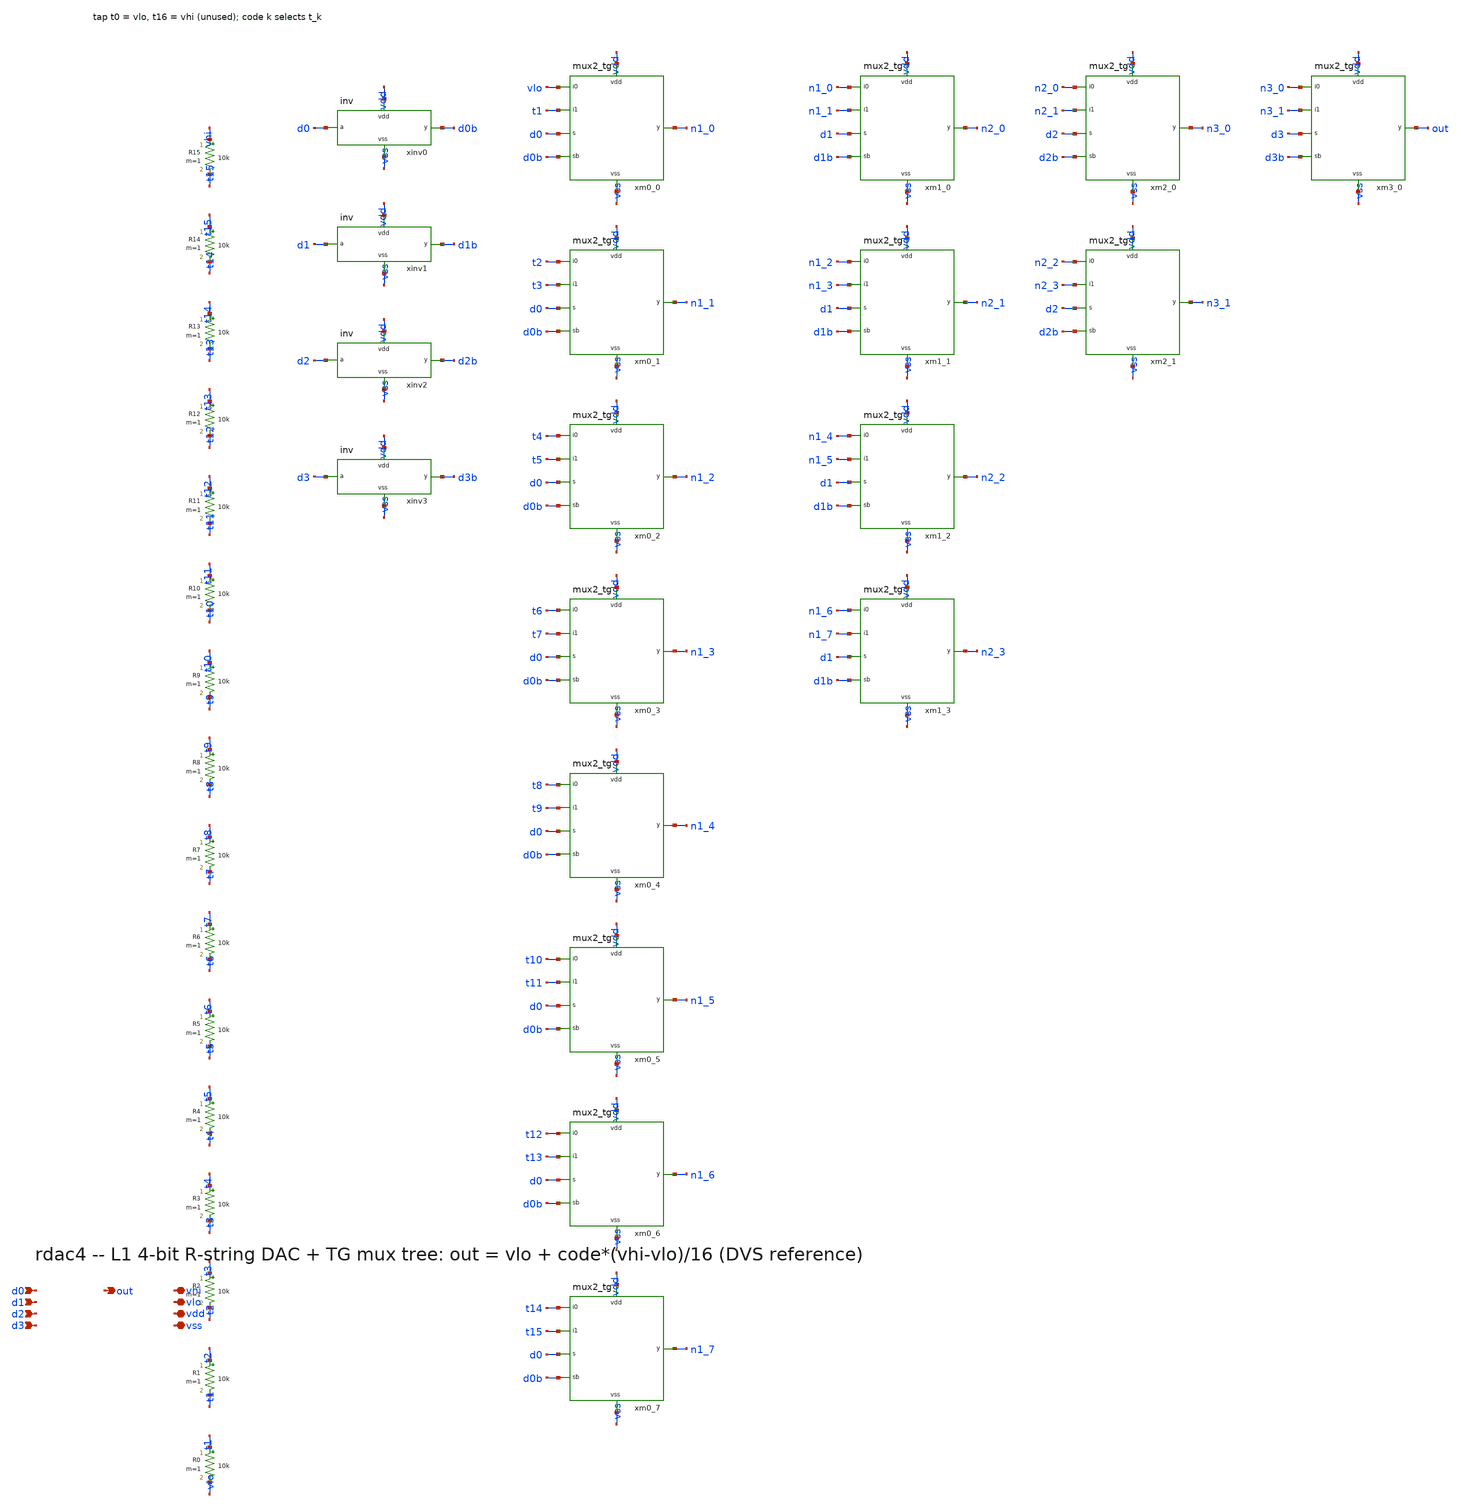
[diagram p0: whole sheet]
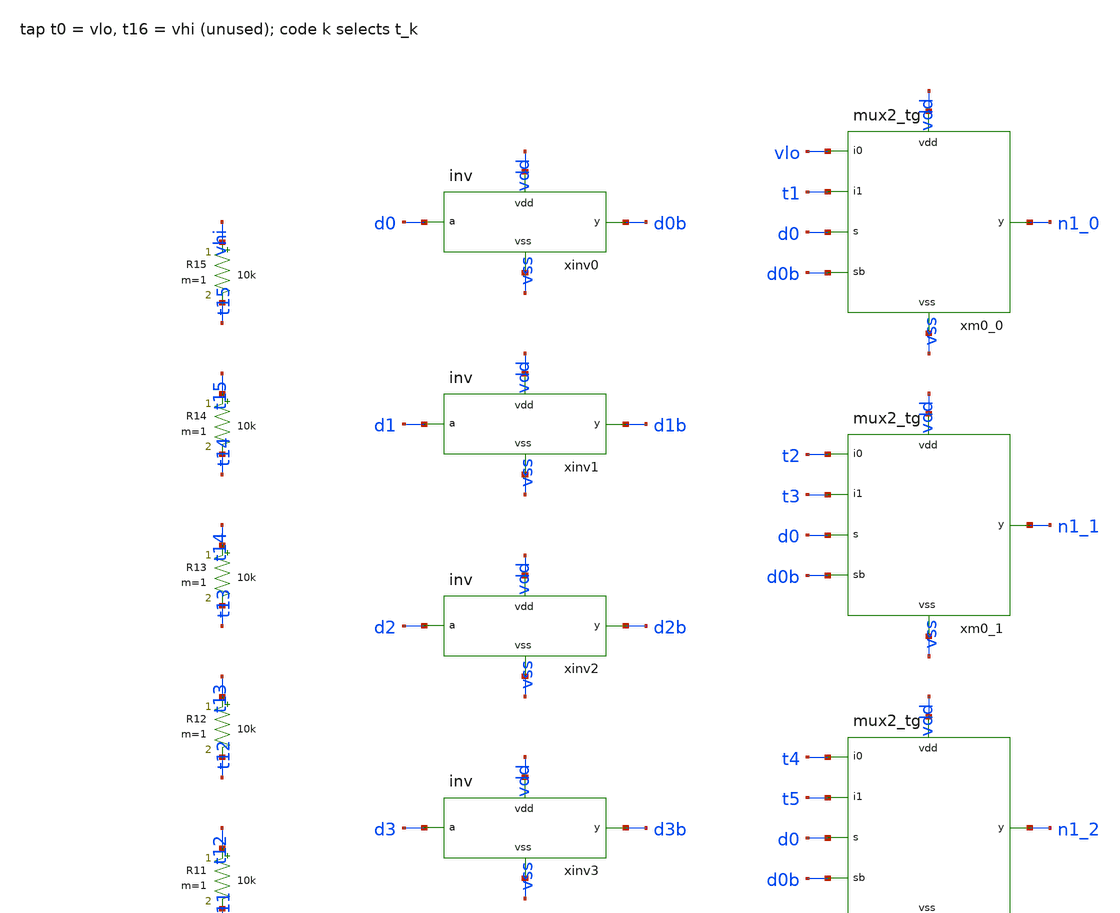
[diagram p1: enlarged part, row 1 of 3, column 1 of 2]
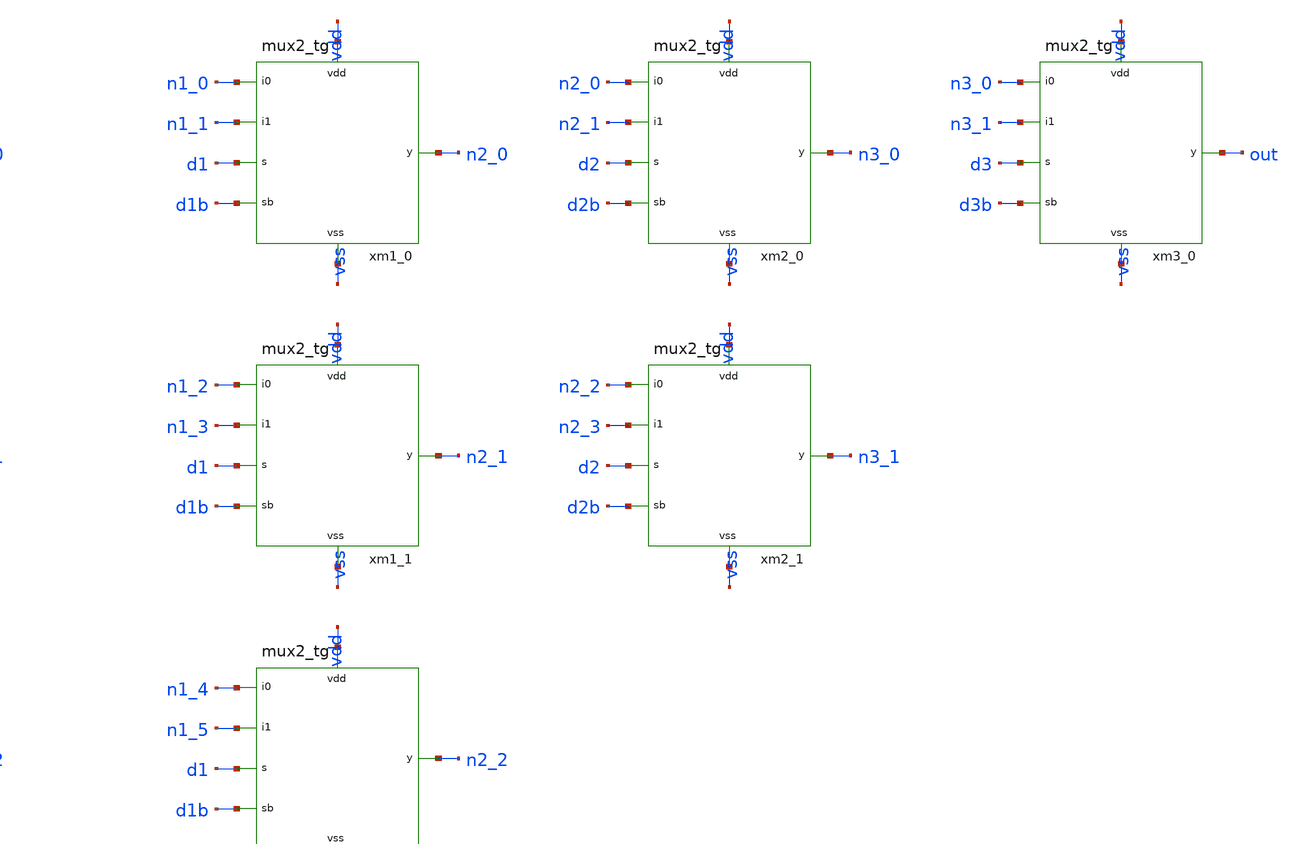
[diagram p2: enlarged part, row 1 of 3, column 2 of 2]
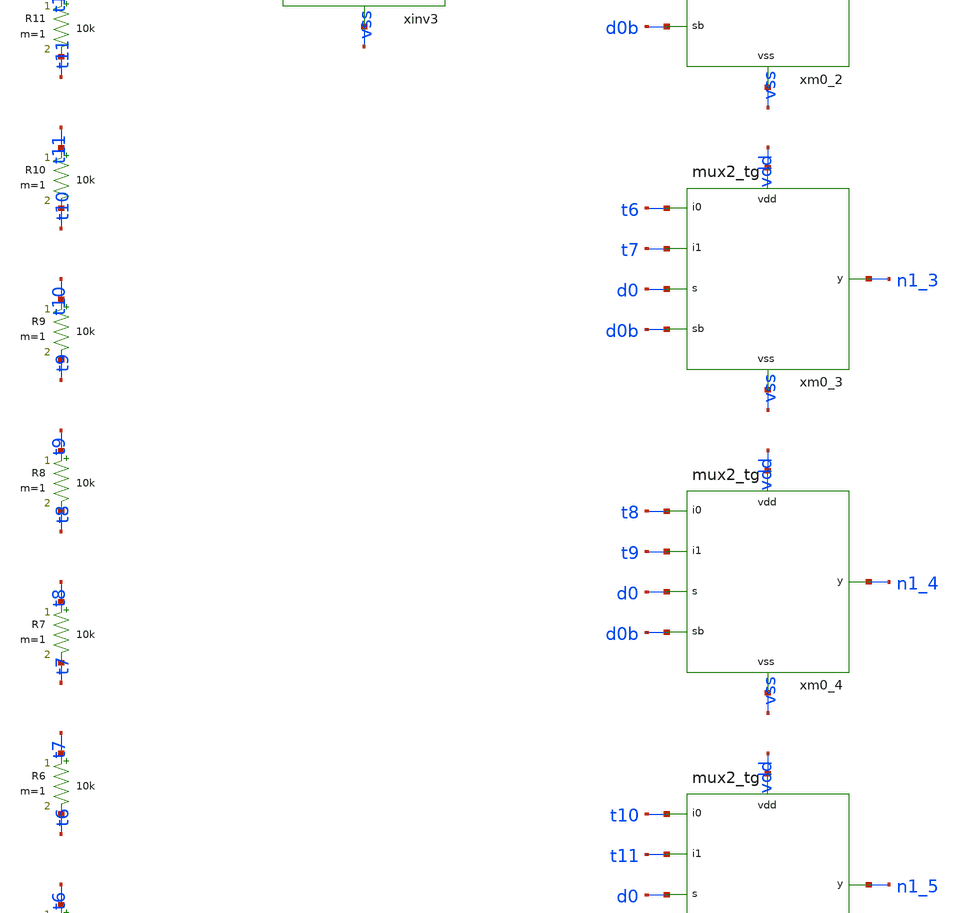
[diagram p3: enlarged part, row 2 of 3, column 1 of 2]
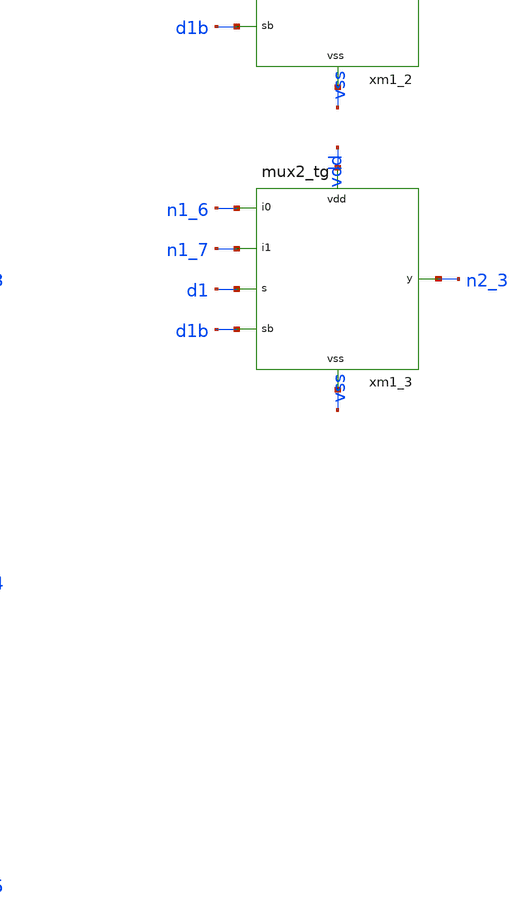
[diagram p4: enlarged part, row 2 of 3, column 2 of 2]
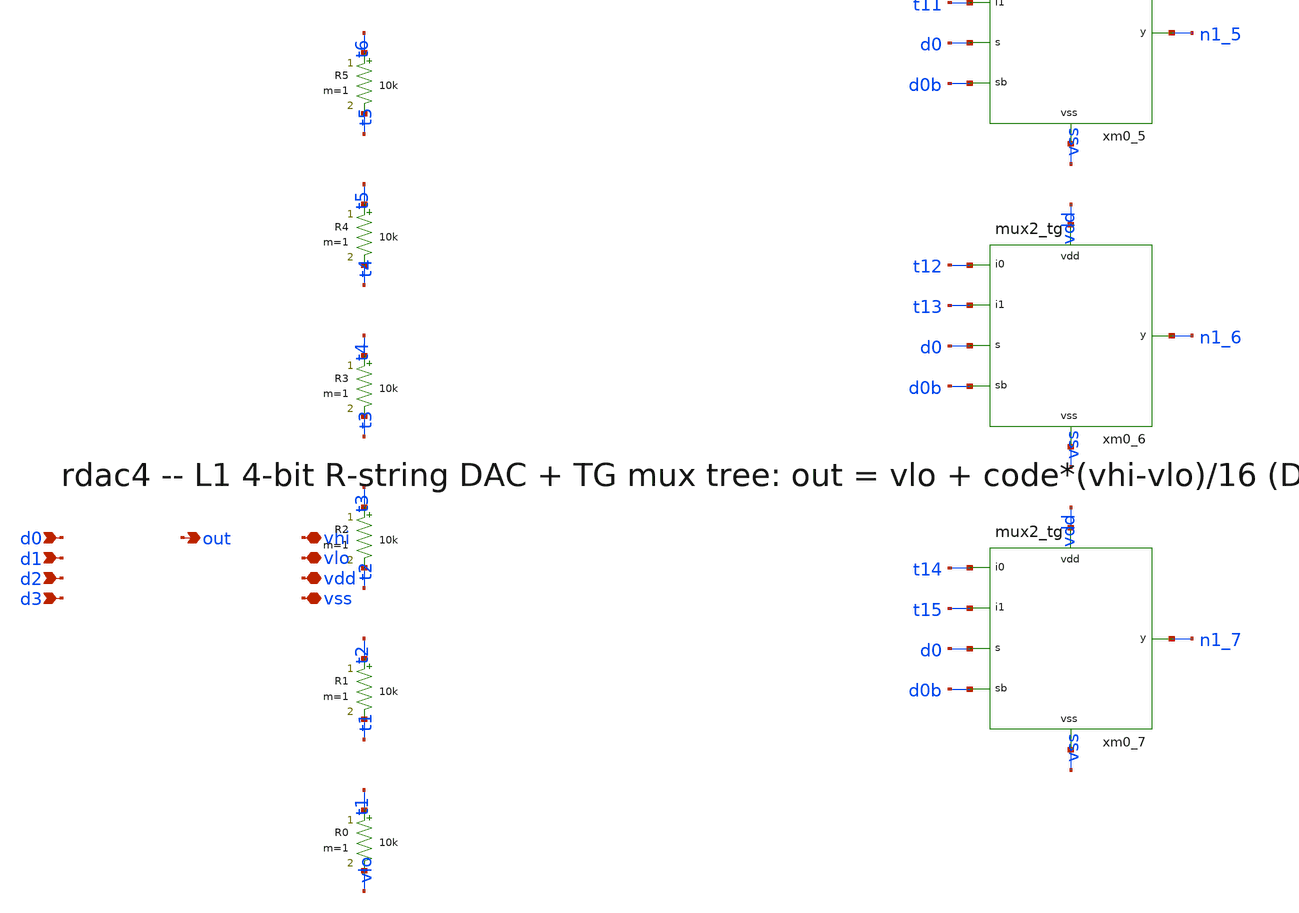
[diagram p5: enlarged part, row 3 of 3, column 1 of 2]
** sch_path: xschem/onetops/rdac4.sch
**.subckt rdac4 d0 d1 d2 d3 out vhi vlo vdd vss
*.ipin d0
*.ipin d1
*.ipin d2
*.ipin d3
*.opin out
*.iopin vhi
*.iopin vlo
*.iopin vdd
*.iopin vss
R0 t1 vlo 10k m=1
R1 t2 t1 10k m=1
R2 t3 t2 10k m=1
R3 t4 t3 10k m=1
R4 t5 t4 10k m=1
R5 t6 t5 10k m=1
R6 t7 t6 10k m=1
R7 t8 t7 10k m=1
R8 t9 t8 10k m=1
R9 t10 t9 10k m=1
R10 t11 t10 10k m=1
R11 t12 t11 10k m=1
R12 t13 t12 10k m=1
R13 t14 t13 10k m=1
R14 t15 t14 10k m=1
R15 vhi t15 10k m=1
xinv0 d0 d0b vdd vss inv
xinv1 d1 d1b vdd vss inv
xinv2 d2 d2b vdd vss inv
xinv3 d3 d3b vdd vss inv
xm0_0 vlo t1 d0 d0b n1_0 vdd vss mux2_tg
xm0_1 t2 t3 d0 d0b n1_1 vdd vss mux2_tg
xm0_2 t4 t5 d0 d0b n1_2 vdd vss mux2_tg
xm0_3 t6 t7 d0 d0b n1_3 vdd vss mux2_tg
xm0_4 t8 t9 d0 d0b n1_4 vdd vss mux2_tg
xm0_5 t10 t11 d0 d0b n1_5 vdd vss mux2_tg
xm0_6 t12 t13 d0 d0b n1_6 vdd vss mux2_tg
xm0_7 t14 t15 d0 d0b n1_7 vdd vss mux2_tg
xm1_0 n1_0 n1_1 d1 d1b n2_0 vdd vss mux2_tg
xm1_1 n1_2 n1_3 d1 d1b n2_1 vdd vss mux2_tg
xm1_2 n1_4 n1_5 d1 d1b n2_2 vdd vss mux2_tg
xm1_3 n1_6 n1_7 d1 d1b n2_3 vdd vss mux2_tg
xm2_0 n2_0 n2_1 d2 d2b n3_0 vdd vss mux2_tg
xm2_1 n2_2 n2_3 d2 d2b n3_1 vdd vss mux2_tg
xm3_0 n3_0 n3_1 d3 d3b out vdd vss mux2_tg
**.ends

* expanding   symbol:  onetops/inv.sym # of pins=4
** sym_path: xschem/onetops/inv.sym
** sch_path: xschem/onetops/inv.sch
.subckt inv a y vdd vss
*.ipin a
*.opin y
*.iopin vdd
*.iopin vss
XMP1 y a vdd vdd sky130_fd_pr__pfet_01v8 L=0.15 W=2 nf=1 ad='int((1 + 1)/2) * 2 / 1 * 0.29' as='int((1 + 2)/2) * 2 / 1 * 0.29'
+ pd='2*int((1 + 1)/2) * (2 / 1 + 0.29)' ps='2*int((1 + 2)/2) * (2 / 1 + 0.29)' nrd='0.29 / 2 ' nrs='0.29 / 2 '
+ sa=0 sb=0 sd=0 mult=1 m=1
XMN1 y a vss vss sky130_fd_pr__nfet_01v8 L=0.15 W=1 nf=1 ad='int((1 + 1)/2) * 1 / 1 * 0.29' as='int((1 + 2)/2) * 1 / 1 * 0.29'
+ pd='2*int((1 + 1)/2) * (1 / 1 + 0.29)' ps='2*int((1 + 2)/2) * (1 / 1 + 0.29)' nrd='0.29 / 1 ' nrs='0.29 / 1 '
+ sa=0 sb=0 sd=0 mult=1 m=1
.ends


* expanding   symbol:  onetops/mux2_tg.sym # of pins=7
** sym_path: xschem/onetops/mux2_tg.sym
** sch_path: xschem/onetops/mux2_tg.sch
.subckt mux2_tg i0 i1 s sb y vdd vss
*.ipin s
*.ipin sb
*.iopin i0
*.iopin i1
*.iopin y
*.iopin vdd
*.iopin vss
xt0 i0 sb s y vdd vss tgate
xt1 i1 s sb y vdd vss tgate
.ends


* expanding   symbol:  onetops/tgate.sym # of pins=6
** sym_path: xschem/onetops/tgate.sym
** sch_path: xschem/onetops/tgate.sch
.subckt tgate a en enb b vdd vss
*.ipin en
*.ipin enb
*.iopin a
*.iopin b
*.iopin vdd
*.iopin vss
XMN1 a en b vss sky130_fd_pr__nfet_01v8 L=0.15 W=1 nf=1 ad='int((1 + 1)/2) * 1 / 1 * 0.29' as='int((1 + 2)/2) * 1 / 1 * 0.29'
+ pd='2*int((1 + 1)/2) * (1 / 1 + 0.29)' ps='2*int((1 + 2)/2) * (1 / 1 + 0.29)' nrd='0.29 / 1 ' nrs='0.29 / 1 '
+ sa=0 sb=0 sd=0 mult=1 m=1
XMP1 b enb a vdd sky130_fd_pr__pfet_01v8 L=0.15 W=2 nf=1 ad='int((1 + 1)/2) * 2 / 1 * 0.29' as='int((1 + 2)/2) * 2 / 1 * 0.29'
+ pd='2*int((1 + 1)/2) * (2 / 1 + 0.29)' ps='2*int((1 + 2)/2) * (2 / 1 + 0.29)' nrd='0.29 / 2 ' nrs='0.29 / 2 '
+ sa=0 sb=0 sd=0 mult=1 m=1
.ends

.end
